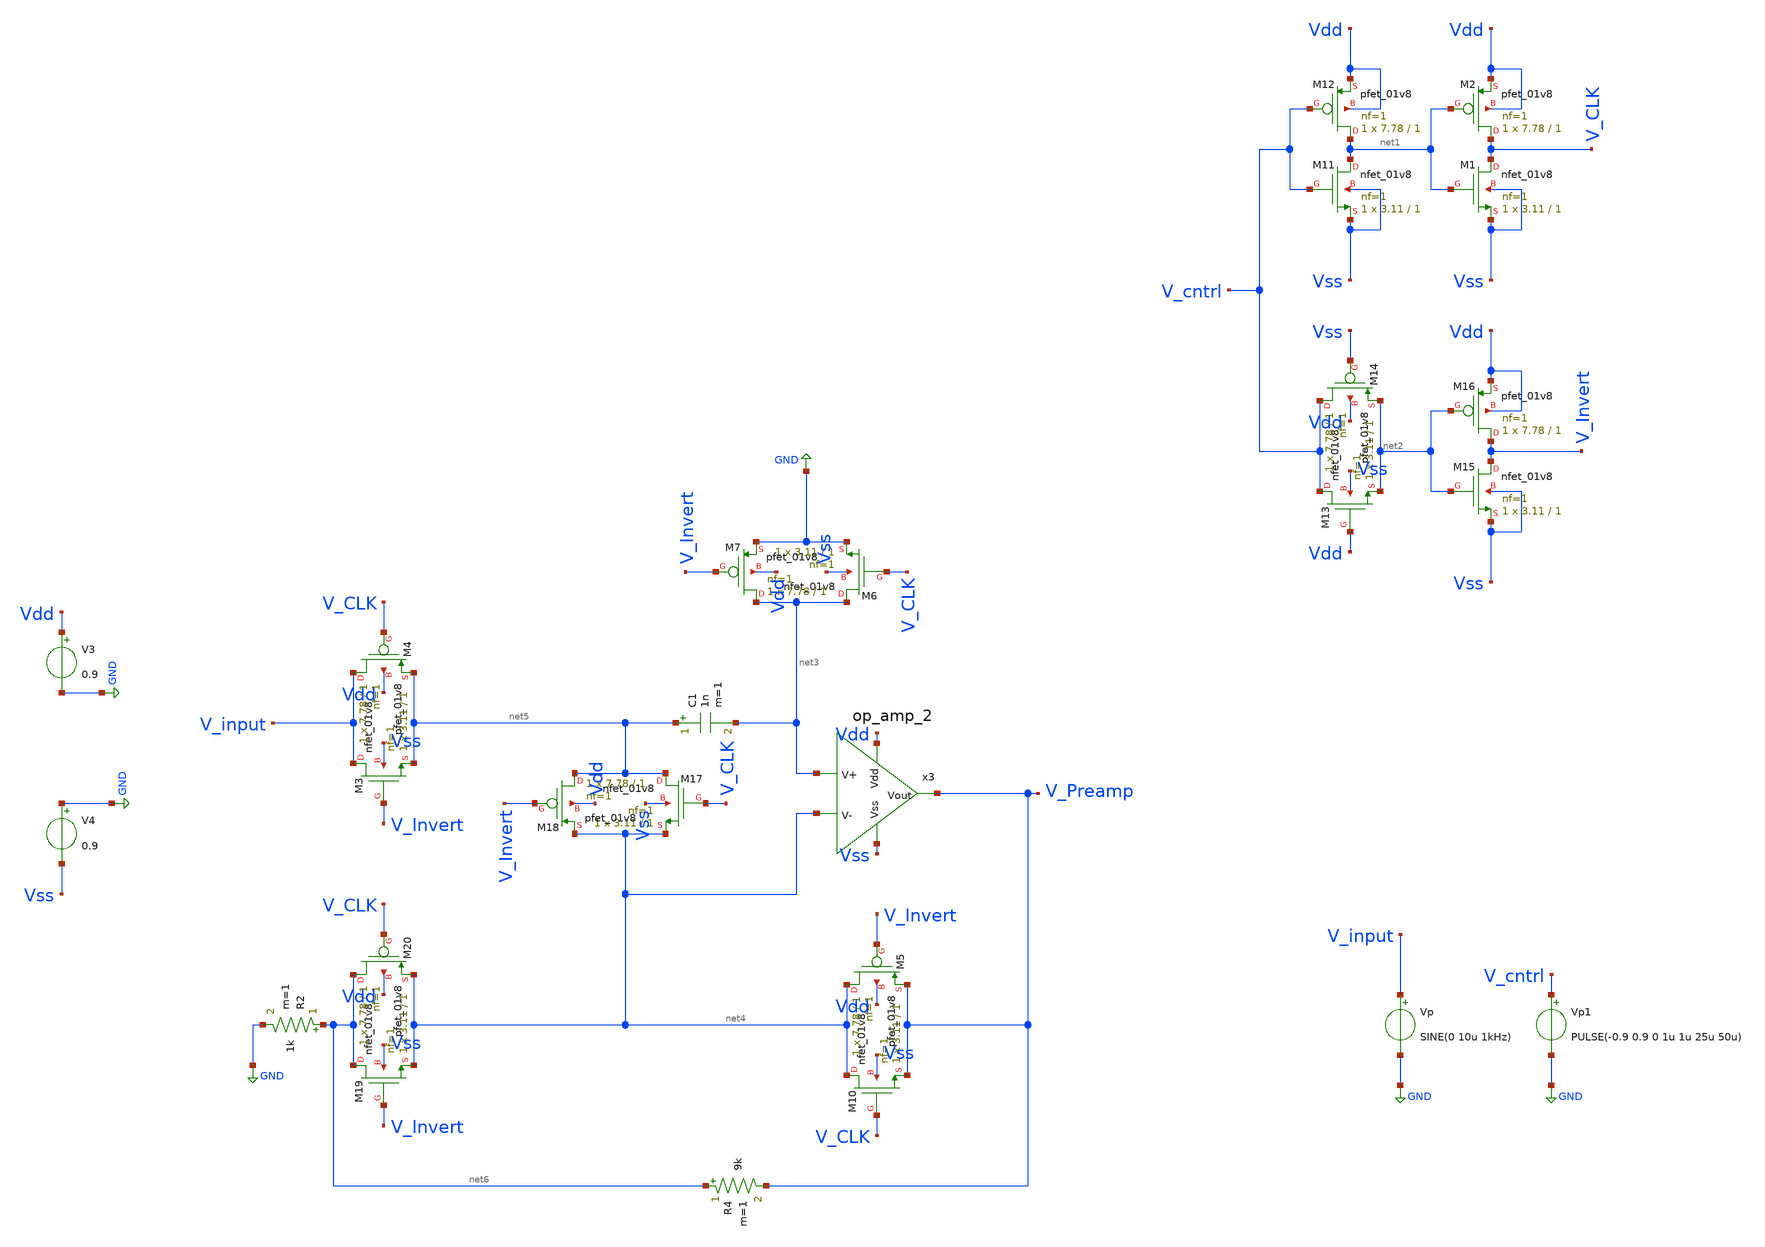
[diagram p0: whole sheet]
** sch_path: xschem/AZERO.sch
**.subckt AZERO
XM1 V_CLK net1 Vss Vss sky130_fd_pr__nfet_01v8 L=1 W=3.11 nf=1 ad='int((1 + 1)/2) * 3.11 / 1 * 0.29'
+ as='int((1 + 2)/2) * 3.11 / 1 * 0.29' pd='2*int((1 + 1)/2) * (3.11 / 1 + 0.29)' ps='2*int((1 + 2)/2) * (3.11 / 1 + 0.29)'
+ nrd='0.29 / 3.11 ' nrs='0.29 / 3.11 ' sa=0 sb=0 sd=0 mult=1 m=1
XM2 V_CLK net1 Vdd Vdd sky130_fd_pr__pfet_01v8 L=1 W=7.78 nf=1 ad='int((1 + 1)/2) * 7.78 / 1 * 0.29'
+ as='int((1 + 2)/2) * 7.78 / 1 * 0.29' pd='2*int((1 + 1)/2) * (7.78 / 1 + 0.29)' ps='2*int((1 + 2)/2) * (7.78 / 1 + 0.29)'
+ nrd='0.29 / 7.78 ' nrs='0.29 / 7.78 ' sa=0 sb=0 sd=0 mult=1 m=1
XM11 net1 V_cntrl Vss Vss sky130_fd_pr__nfet_01v8 L=1 W=3.11 nf=1 ad='int((1 + 1)/2) * 3.11 / 1 * 0.29'
+ as='int((1 + 2)/2) * 3.11 / 1 * 0.29' pd='2*int((1 + 1)/2) * (3.11 / 1 + 0.29)' ps='2*int((1 + 2)/2) * (3.11 / 1 + 0.29)'
+ nrd='0.29 / 3.11 ' nrs='0.29 / 3.11 ' sa=0 sb=0 sd=0 mult=1 m=1
XM12 net1 V_cntrl Vdd Vdd sky130_fd_pr__pfet_01v8 L=1 W=7.78 nf=1 ad='int((1 + 1)/2) * 7.78 / 1 * 0.29'
+ as='int((1 + 2)/2) * 7.78 / 1 * 0.29' pd='2*int((1 + 1)/2) * (7.78 / 1 + 0.29)' ps='2*int((1 + 2)/2) * (7.78 / 1 + 0.29)'
+ nrd='0.29 / 7.78 ' nrs='0.29 / 7.78 ' sa=0 sb=0 sd=0 mult=1 m=1
XM13 V_cntrl Vdd net2 Vss sky130_fd_pr__nfet_01v8 L=1 W=3.11 nf=1 ad='int((1 + 1)/2) * 3.11 / 1 * 0.29'
+ as='int((1 + 2)/2) * 3.11 / 1 * 0.29' pd='2*int((1 + 1)/2) * (3.11 / 1 + 0.29)' ps='2*int((1 + 2)/2) * (3.11 / 1 + 0.29)'
+ nrd='0.29 / 3.11 ' nrs='0.29 / 3.11 ' sa=0 sb=0 sd=0 mult=1 m=1
XM14 V_cntrl Vss net2 Vdd sky130_fd_pr__pfet_01v8 L=1 W=7.78 nf=1 ad='int((1 + 1)/2) * 7.78 / 1 * 0.29'
+ as='int((1 + 2)/2) * 7.78 / 1 * 0.29' pd='2*int((1 + 1)/2) * (7.78 / 1 + 0.29)' ps='2*int((1 + 2)/2) * (7.78 / 1 + 0.29)'
+ nrd='0.29 / 7.78 ' nrs='0.29 / 7.78 ' sa=0 sb=0 sd=0 mult=1 m=1
XM15 V_Invert net2 Vss Vss sky130_fd_pr__nfet_01v8 L=1 W=3.11 nf=1 ad='int((1 + 1)/2) * 3.11 / 1 * 0.29'
+ as='int((1 + 2)/2) * 3.11 / 1 * 0.29' pd='2*int((1 + 1)/2) * (3.11 / 1 + 0.29)' ps='2*int((1 + 2)/2) * (3.11 / 1 + 0.29)'
+ nrd='0.29 / 3.11 ' nrs='0.29 / 3.11 ' sa=0 sb=0 sd=0 mult=1 m=1
XM16 V_Invert net2 Vdd Vdd sky130_fd_pr__pfet_01v8 L=1 W=7.78 nf=1 ad='int((1 + 1)/2) * 7.78 / 1 * 0.29'
+ as='int((1 + 2)/2) * 7.78 / 1 * 0.29' pd='2*int((1 + 1)/2) * (7.78 / 1 + 0.29)' ps='2*int((1 + 2)/2) * (7.78 / 1 + 0.29)'
+ nrd='0.29 / 7.78 ' nrs='0.29 / 7.78 ' sa=0 sb=0 sd=0 mult=1 m=1
x3 Vdd V_Preamp net3 net4 Vss op_amp_2
R2 net6 GND 1k m=1
R4 net6 V_Preamp 9k m=1
Vp V_input GND SINE(0 10u 1kHz)
Vp1 V_cntrl GND PULSE(-0.9 0.9 0 1u 1u 25u 50u)
V4 GND Vss 0.9
V3 Vdd GND 0.9
XM10 net4 V_CLK V_Preamp Vss sky130_fd_pr__nfet_01v8 L=1 W=3.11 nf=1 ad='int((1 + 1)/2) * 3.11 / 1 * 0.29'
+ as='int((1 + 2)/2) * 3.11 / 1 * 0.29' pd='2*int((1 + 1)/2) * (3.11 / 1 + 0.29)' ps='2*int((1 + 2)/2) * (3.11 / 1 + 0.29)'
+ nrd='0.29 / 3.11 ' nrs='0.29 / 3.11 ' sa=0 sb=0 sd=0 mult=1 m=1
XM5 net4 V_Invert V_Preamp Vdd sky130_fd_pr__pfet_01v8 L=1 W=7.78 nf=1 ad='int((1 + 1)/2) * 7.78 / 1 * 0.29'
+ as='int((1 + 2)/2) * 7.78 / 1 * 0.29' pd='2*int((1 + 1)/2) * (7.78 / 1 + 0.29)' ps='2*int((1 + 2)/2) * (7.78 / 1 + 0.29)'
+ nrd='0.29 / 7.78 ' nrs='0.29 / 7.78 ' sa=0 sb=0 sd=0 mult=1 m=1
XM3 V_input V_Invert net5 Vss sky130_fd_pr__nfet_01v8 L=1 W=3.11 nf=1 ad='int((1 + 1)/2) * 3.11 / 1 * 0.29'
+ as='int((1 + 2)/2) * 3.11 / 1 * 0.29' pd='2*int((1 + 1)/2) * (3.11 / 1 + 0.29)' ps='2*int((1 + 2)/2) * (3.11 / 1 + 0.29)'
+ nrd='0.29 / 3.11 ' nrs='0.29 / 3.11 ' sa=0 sb=0 sd=0 mult=1 m=1
XM4 V_input V_CLK net5 Vdd sky130_fd_pr__pfet_01v8 L=1 W=7.78 nf=1 ad='int((1 + 1)/2) * 7.78 / 1 * 0.29'
+ as='int((1 + 2)/2) * 7.78 / 1 * 0.29' pd='2*int((1 + 1)/2) * (7.78 / 1 + 0.29)' ps='2*int((1 + 2)/2) * (7.78 / 1 + 0.29)'
+ nrd='0.29 / 7.78 ' nrs='0.29 / 7.78 ' sa=0 sb=0 sd=0 mult=1 m=1
XM17 net5 V_CLK net4 Vss sky130_fd_pr__nfet_01v8 L=1 W=3.11 nf=1 ad='int((1 + 1)/2) * 3.11 / 1 * 0.29'
+ as='int((1 + 2)/2) * 3.11 / 1 * 0.29' pd='2*int((1 + 1)/2) * (3.11 / 1 + 0.29)' ps='2*int((1 + 2)/2) * (3.11 / 1 + 0.29)'
+ nrd='0.29 / 3.11 ' nrs='0.29 / 3.11 ' sa=0 sb=0 sd=0 mult=1 m=1
XM18 net5 V_Invert net4 Vdd sky130_fd_pr__pfet_01v8 L=1 W=7.78 nf=1 ad='int((1 + 1)/2) * 7.78 / 1 * 0.29'
+ as='int((1 + 2)/2) * 7.78 / 1 * 0.29' pd='2*int((1 + 1)/2) * (7.78 / 1 + 0.29)' ps='2*int((1 + 2)/2) * (7.78 / 1 + 0.29)'
+ nrd='0.29 / 7.78 ' nrs='0.29 / 7.78 ' sa=0 sb=0 sd=0 mult=1 m=1
C1 net5 net3 1n m=1
XM19 net6 V_Invert net4 Vss sky130_fd_pr__nfet_01v8 L=1 W=3.11 nf=1 ad='int((1 + 1)/2) * 3.11 / 1 * 0.29'
+ as='int((1 + 2)/2) * 3.11 / 1 * 0.29' pd='2*int((1 + 1)/2) * (3.11 / 1 + 0.29)' ps='2*int((1 + 2)/2) * (3.11 / 1 + 0.29)'
+ nrd='0.29 / 3.11 ' nrs='0.29 / 3.11 ' sa=0 sb=0 sd=0 mult=1 m=1
XM20 net6 V_CLK net4 Vdd sky130_fd_pr__pfet_01v8 L=1 W=7.78 nf=1 ad='int((1 + 1)/2) * 7.78 / 1 * 0.29'
+ as='int((1 + 2)/2) * 7.78 / 1 * 0.29' pd='2*int((1 + 1)/2) * (7.78 / 1 + 0.29)' ps='2*int((1 + 2)/2) * (7.78 / 1 + 0.29)'
+ nrd='0.29 / 7.78 ' nrs='0.29 / 7.78 ' sa=0 sb=0 sd=0 mult=1 m=1
XM6 net3 V_CLK GND Vss sky130_fd_pr__nfet_01v8 L=1 W=3.11 nf=1 ad='int((1 + 1)/2) * 3.11 / 1 * 0.29'
+ as='int((1 + 2)/2) * 3.11 / 1 * 0.29' pd='2*int((1 + 1)/2) * (3.11 / 1 + 0.29)' ps='2*int((1 + 2)/2) * (3.11 / 1 + 0.29)'
+ nrd='0.29 / 3.11 ' nrs='0.29 / 3.11 ' sa=0 sb=0 sd=0 mult=1 m=1
XM7 net3 V_Invert GND Vdd sky130_fd_pr__pfet_01v8 L=1 W=7.78 nf=1 ad='int((1 + 1)/2) * 7.78 / 1 * 0.29'
+ as='int((1 + 2)/2) * 7.78 / 1 * 0.29' pd='2*int((1 + 1)/2) * (7.78 / 1 + 0.29)' ps='2*int((1 + 2)/2) * (7.78 / 1 + 0.29)'
+ nrd='0.29 / 7.78 ' nrs='0.29 / 7.78 ' sa=0 sb=0 sd=0 mult=1 m=1
**** begin user architecture code


.lib /foss/pdks/sky130A/libs.tech/combined/sky130.lib.spice tt
.control
 tran 0.1u 2m
 plot v(V_input)
 plot v(V_CLK) v(V_Invert)
 plot v(V_Preamp) title 'AutoZero Output Gain:10'
 plot v(V_input) v(V_Preamp) title 'AutoZero Input:10uV Gain:10 Offset approx: 4.5uV (x100 less offset than non-azero op amp)'
 *noise v(V_out2) Vp dec 10 1 1MEG
.endc
.end

**** end user architecture code
**.ends

* expanding   symbol:  op_amp_2.sym # of pins=5
** sym_path: xschem/op_amp_2.sym
** sch_path: xschem/op_amp_2.sch
.subckt op_amp_2 Vdd Vout V+ V- Vss
*.opin Vout
*.ipin Vdd
*.ipin Vss
*.ipin V+
*.ipin V-
XM1 net1 net1 Vss Vss sky130_fd_pr__nfet_01v8 L=1 W=9.35 nf=1 ad='int((1 + 1)/2) * 9.35 / 1 * 0.29' as='int((1 + 2)/2) * 9.35 / 1 * 0.29'
+ pd='2*int((1 + 1)/2) * (9.35 / 1 + 0.29)' ps='2*int((1 + 2)/2) * (9.35 / 1 + 0.29)' nrd='0.29 / 9.35 '
+ nrs='0.29 / 9.35 ' sa=0 sb=0 sd=0 mult=1 m=1
XM3 net2 net1 Vss Vss sky130_fd_pr__nfet_01v8 L=1 W=9.35 nf=1 ad='int((1 + 1)/2) * 9.35 / 1 * 0.29' as='int((1 + 2)/2) * 9.35 / 1 * 0.29'
+ pd='2*int((1 + 1)/2) * (9.35 / 1 + 0.29)' ps='2*int((1 + 2)/2) * (9.35 / 1 + 0.29)' nrd='0.29 / 9.35 '
+ nrs='0.29 / 9.35 ' sa=0 sb=0 sd=0 mult=1 m=1
XM10 net3 V- net2 Vss sky130_fd_pr__nfet_01v8 L=1 W=3.11 nf=1 ad='int((1 + 1)/2) * 3.11 / 1 * 0.29' as='int((1 + 2)/2) * 3.11 / 1 * 0.29'
+ pd='2*int((1 + 1)/2) * (3.11 / 1 + 0.29)' ps='2*int((1 + 2)/2) * (3.11 / 1 + 0.29)' nrd='0.29 / 3.11 '
+ nrs='0.29 / 3.11 ' sa=0 sb=0 sd=0 mult=1 m=1
XM11 net4 V+ net2 Vss sky130_fd_pr__nfet_01v8 L=1 W=3.11 nf=1 ad='int((1 + 1)/2) * 3.11 / 1 * 0.29' as='int((1 + 2)/2) * 3.11 / 1 * 0.29'
+ pd='2*int((1 + 1)/2) * (3.11 / 1 + 0.29)' ps='2*int((1 + 2)/2) * (3.11 / 1 + 0.29)' nrd='0.29 / 3.11 '
+ nrs='0.29 / 3.11 ' sa=0 sb=0 sd=0 mult=1 m=1
XM5 net4 net3 Vdd Vdd sky130_fd_pr__pfet_01v8 L=1 W=3.41 nf=1 ad='int((1 + 1)/2) * 3.41 / 1 * 0.29' as='int((1 + 2)/2) * 3.41 / 1 * 0.29'
+ pd='2*int((1 + 1)/2) * (3.41 / 1 + 0.29)' ps='2*int((1 + 2)/2) * (3.41 / 1 + 0.29)' nrd='0.29 / 3.41 '
+ nrs='0.29 / 3.41 ' sa=0 sb=0 sd=0 mult=1 m=1
XM6 net3 net3 Vdd Vdd sky130_fd_pr__pfet_01v8 L=1 W=3.41 nf=1 ad='int((1 + 1)/2) * 3.41 / 1 * 0.29' as='int((1 + 2)/2) * 3.41 / 1 * 0.29'
+ pd='2*int((1 + 1)/2) * (3.41 / 1 + 0.29)' ps='2*int((1 + 2)/2) * (3.41 / 1 + 0.29)' nrd='0.29 / 3.41 '
+ nrs='0.29 / 3.41 ' sa=0 sb=0 sd=0 mult=1 m=1
C1 Vout net4 500f m=1
C2 GND Vout 2p m=1
XM2 net1 net1 Vdd Vdd sky130_fd_pr__pfet_01v8 L=1 W=8.92 nf=1 ad='int((1 + 1)/2) * 8.92 / 1 * 0.29' as='int((1 + 2)/2) * 8.92 / 1 * 0.29'
+ pd='2*int((1 + 1)/2) * (8.92 / 1 + 0.29)' ps='2*int((1 + 2)/2) * (8.92 / 1 + 0.29)' nrd='0.29 / 8.92 '
+ nrs='0.29 / 8.92 ' sa=0 sb=0 sd=0 mult=1 m=1
XM7 Vout net4 Vdd Vdd sky130_fd_pr__pfet_01v8 L=1 W=54.48 nf=1 ad='int((1 + 1)/2) * 54.48 / 1 * 0.29'
+ as='int((1 + 2)/2) * 54.48 / 1 * 0.29' pd='2*int((1 + 1)/2) * (54.48 / 1 + 0.29)' ps='2*int((1 + 2)/2) * (54.48 / 1 + 0.29)'
+ nrd='0.29 / 54.48 ' nrs='0.29 / 54.48 ' sa=0 sb=0 sd=0 mult=1 m=1
XM9 Vout net1 Vss Vss sky130_fd_pr__nfet_01v8 L=1 W=74.77 nf=1 ad='int((1 + 1)/2) * 74.77 / 1 * 0.29'
+ as='int((1 + 2)/2) * 74.77 / 1 * 0.29' pd='2*int((1 + 1)/2) * (74.77 / 1 + 0.29)' ps='2*int((1 + 2)/2) * (74.77 / 1 + 0.29)'
+ nrd='0.29 / 74.77 ' nrs='0.29 / 74.77 ' sa=0 sb=0 sd=0 mult=1 m=1
.ends

.GLOBAL GND
.end
